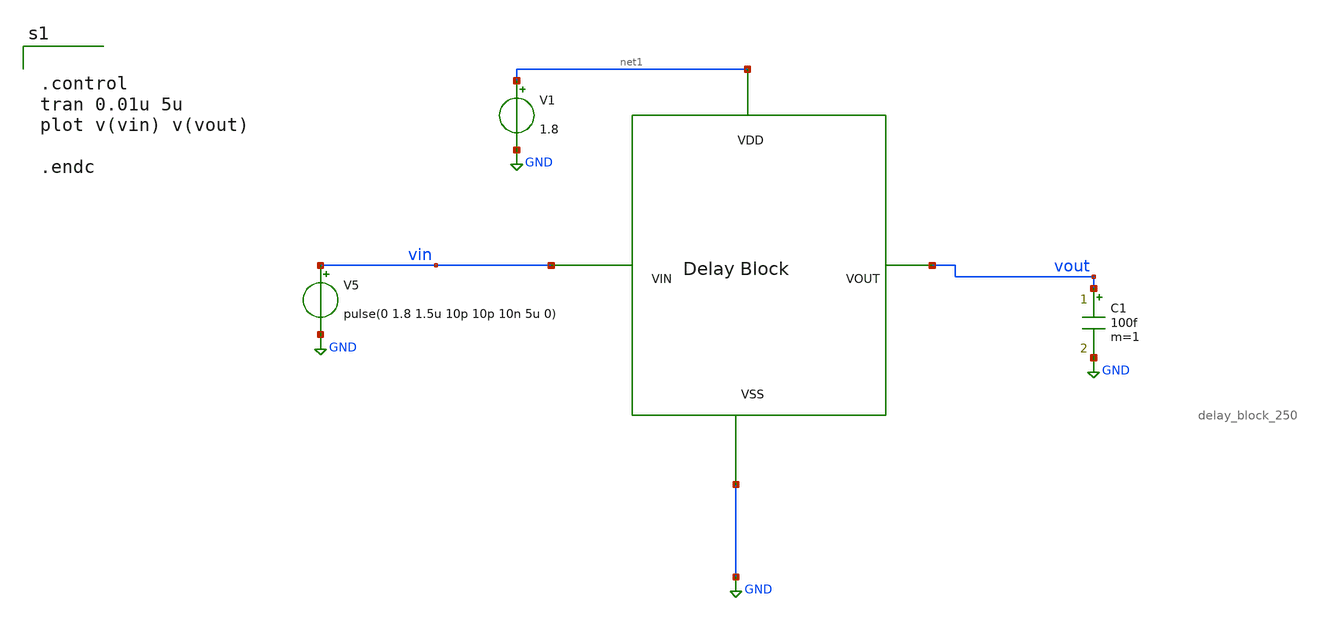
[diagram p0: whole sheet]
** sch_path: xschem/DC_DC_Converter_xschem/OTHERS/DC_DC_Converter_JV11/Delay_block_revised/delay_block_250n_tb.sch
**.subckt delay_block_250n_tb
V1 net1 GND 1.8
V5 vin GND pulse(0 1.8 1.5u 10p 10p 10n 5u 0)
C1 vout GND 100f m=1
x1 net1 vin vout GND delay_block_250
**** begin user architecture code


.control
tran 0.01u 5u
plot v(vin) v(vout)

.endc



** opencircuitdesign pdks install
.lib $::SKYWATER_MODELS/sky130.lib.spice tt


**** end user architecture code
**.ends
.GLOBAL GND
.end
